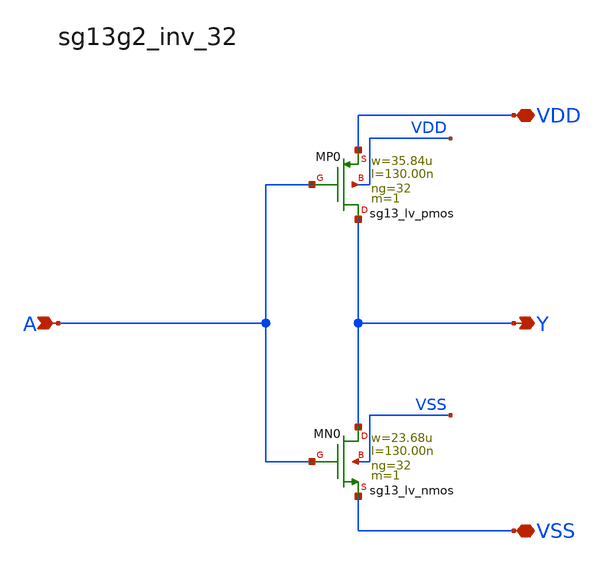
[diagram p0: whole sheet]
** sch_path: outputs/sg13g2_cells/cells/sg13g2_inv_32/sg13g2_inv_32.sch
**.subckt sg13g2_inv_32 Y A VDD VSS
*.opin Y
*.ipin A
*.iopin VDD
*.iopin VSS
XMN0 Y A VSS VSS sg13_lv_nmos w=23.68u l=130.00n ng=32 m=1 mm_ok=1
XMP0 Y A VDD VDD sg13_lv_pmos w=35.84u l=130.00n ng=32 m=1 mm_ok=1
**.ends
.end
